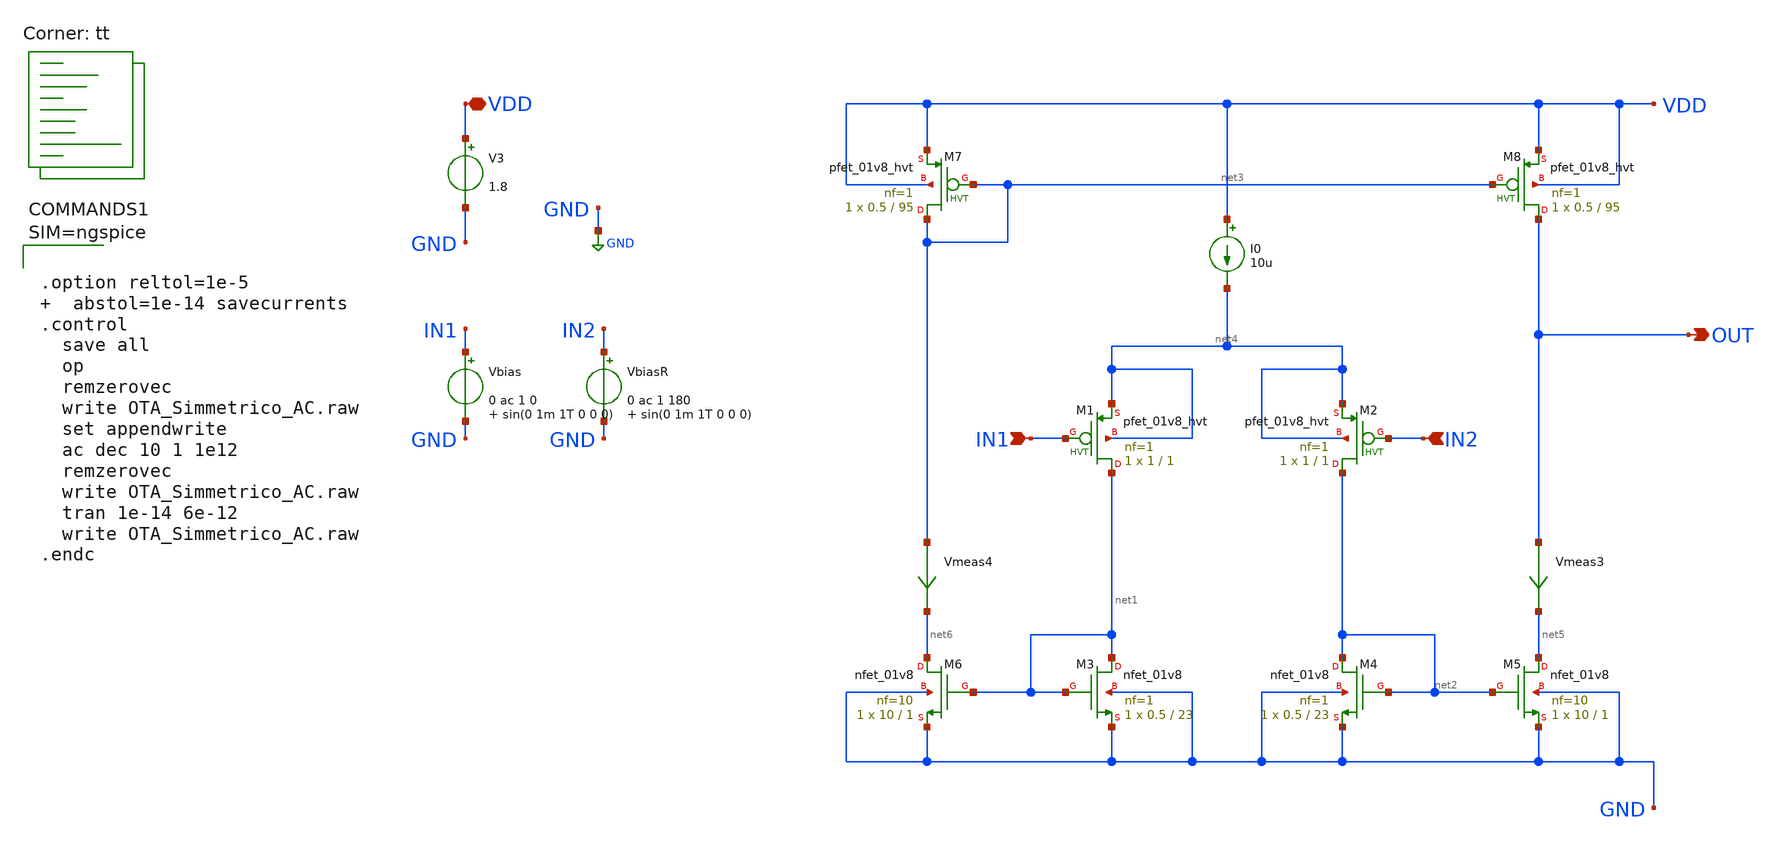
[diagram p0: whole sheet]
** sch_path: xschem/OTA_Simmetrico_AC.sch
**.subckt OTA_Simmetrico_AC VDD IN1 IN2 OUT
*.iopin VDD
*.ipin IN1
*.ipin IN2
*.opin OUT
XM1 net1 IN1 net4 net4 sky130_fd_pr__pfet_01v8_hvt L=1 W=1 nf=1 ad='int((nf+1)/2) * W/nf * 0.29' as='int((nf+2)/2) * W/nf * 0.29'
+ pd='2*int((nf+1)/2) * (W/nf + 0.29)' ps='2*int((nf+2)/2) * (W/nf + 0.29)' nrd='0.29 / W' nrs='0.29 / W'
+ sa=0 sb=0 sd=0 mult=1 m=1
XM2 net2 IN2 net4 net4 sky130_fd_pr__pfet_01v8_hvt L=1 W=1 nf=1 ad='int((nf+1)/2) * W/nf * 0.29' as='int((nf+2)/2) * W/nf * 0.29'
+ pd='2*int((nf+1)/2) * (W/nf + 0.29)' ps='2*int((nf+2)/2) * (W/nf + 0.29)' nrd='0.29 / W' nrs='0.29 / W'
+ sa=0 sb=0 sd=0 mult=1 m=1
XM3 net1 net1 GND GND sky130_fd_pr__nfet_01v8 L=23 W=0.5 nf=1 ad='int((nf+1)/2) * W/nf * 0.29' as='int((nf+2)/2) * W/nf * 0.29'
+ pd='2*int((nf+1)/2) * (W/nf + 0.29)' ps='2*int((nf+2)/2) * (W/nf + 0.29)' nrd='0.29 / W' nrs='0.29 / W'
+ sa=0 sb=0 sd=0 mult=1 m=1
XM4 net2 net2 GND GND sky130_fd_pr__nfet_01v8 L=23 W=0.5 nf=1 ad='int((nf+1)/2) * W/nf * 0.29' as='int((nf+2)/2) * W/nf * 0.29'
+ pd='2*int((nf+1)/2) * (W/nf + 0.29)' ps='2*int((nf+2)/2) * (W/nf + 0.29)' nrd='0.29 / W' nrs='0.29 / W'
+ sa=0 sb=0 sd=0 mult=1 m=1
XM5 net5 net2 GND GND sky130_fd_pr__nfet_01v8 L=1 W=10 nf=10 ad='int((nf+1)/2) * W/nf * 0.29' as='int((nf+2)/2) * W/nf * 0.29'
+ pd='2*int((nf+1)/2) * (W/nf + 0.29)' ps='2*int((nf+2)/2) * (W/nf + 0.29)' nrd='0.29 / W' nrs='0.29 / W'
+ sa=0 sb=0 sd=0 mult=1 m=1
XM6 net6 net1 GND GND sky130_fd_pr__nfet_01v8 L=1 W=10 nf=10 ad='int((nf+1)/2) * W/nf * 0.29' as='int((nf+2)/2) * W/nf * 0.29'
+ pd='2*int((nf+1)/2) * (W/nf + 0.29)' ps='2*int((nf+2)/2) * (W/nf + 0.29)' nrd='0.29 / W' nrs='0.29 / W'
+ sa=0 sb=0 sd=0 mult=1 m=1
XM7 net3 net3 VDD VDD sky130_fd_pr__pfet_01v8_hvt L=95 W=0.5 nf=1 ad='int((nf+1)/2) * W/nf * 0.29' as='int((nf+2)/2) * W/nf * 0.29'
+ pd='2*int((nf+1)/2) * (W/nf + 0.29)' ps='2*int((nf+2)/2) * (W/nf + 0.29)' nrd='0.29 / W' nrs='0.29 / W'
+ sa=0 sb=0 sd=0 mult=1 m=1
XM8 OUT net3 VDD VDD sky130_fd_pr__pfet_01v8_hvt L=95 W=0.5 nf=1 ad='int((nf+1)/2) * W/nf * 0.29' as='int((nf+2)/2) * W/nf * 0.29'
+ pd='2*int((nf+1)/2) * (W/nf + 0.29)' ps='2*int((nf+2)/2) * (W/nf + 0.29)' nrd='0.29 / W' nrs='0.29 / W'
+ sa=0 sb=0 sd=0 mult=1 m=1
Vmeas3 OUT net5 0
.save i(vmeas3)
Vmeas4 net3 net6 0
.save i(vmeas4)
V3 VDD GND 1.8
Vbias IN1 GND 0 ac 1 0 sin(0 1m 1T 0 0 0)
VbiasR IN2 GND 0 ac 1 180 sin(0 1m 1T 0 0 0)
I0 VDD net4 10u
**** begin user architecture code
.lib $::SKYWATER_MODELS/sky130.lib.spice tt



.option reltol=1e-5   abstol=1e-14 savecurrents
.control
  save all
  op
  remzerovec
  write OTA_Simmetrico_AC.raw
  set appendwrite
  ac dec 10 1 1e12
  remzerovec
  write OTA_Simmetrico_AC.raw
  tran 1e-14 6e-12
  write OTA_Simmetrico_AC.raw
.endc



**** end user architecture code
**.ends
.GLOBAL GND
.end
